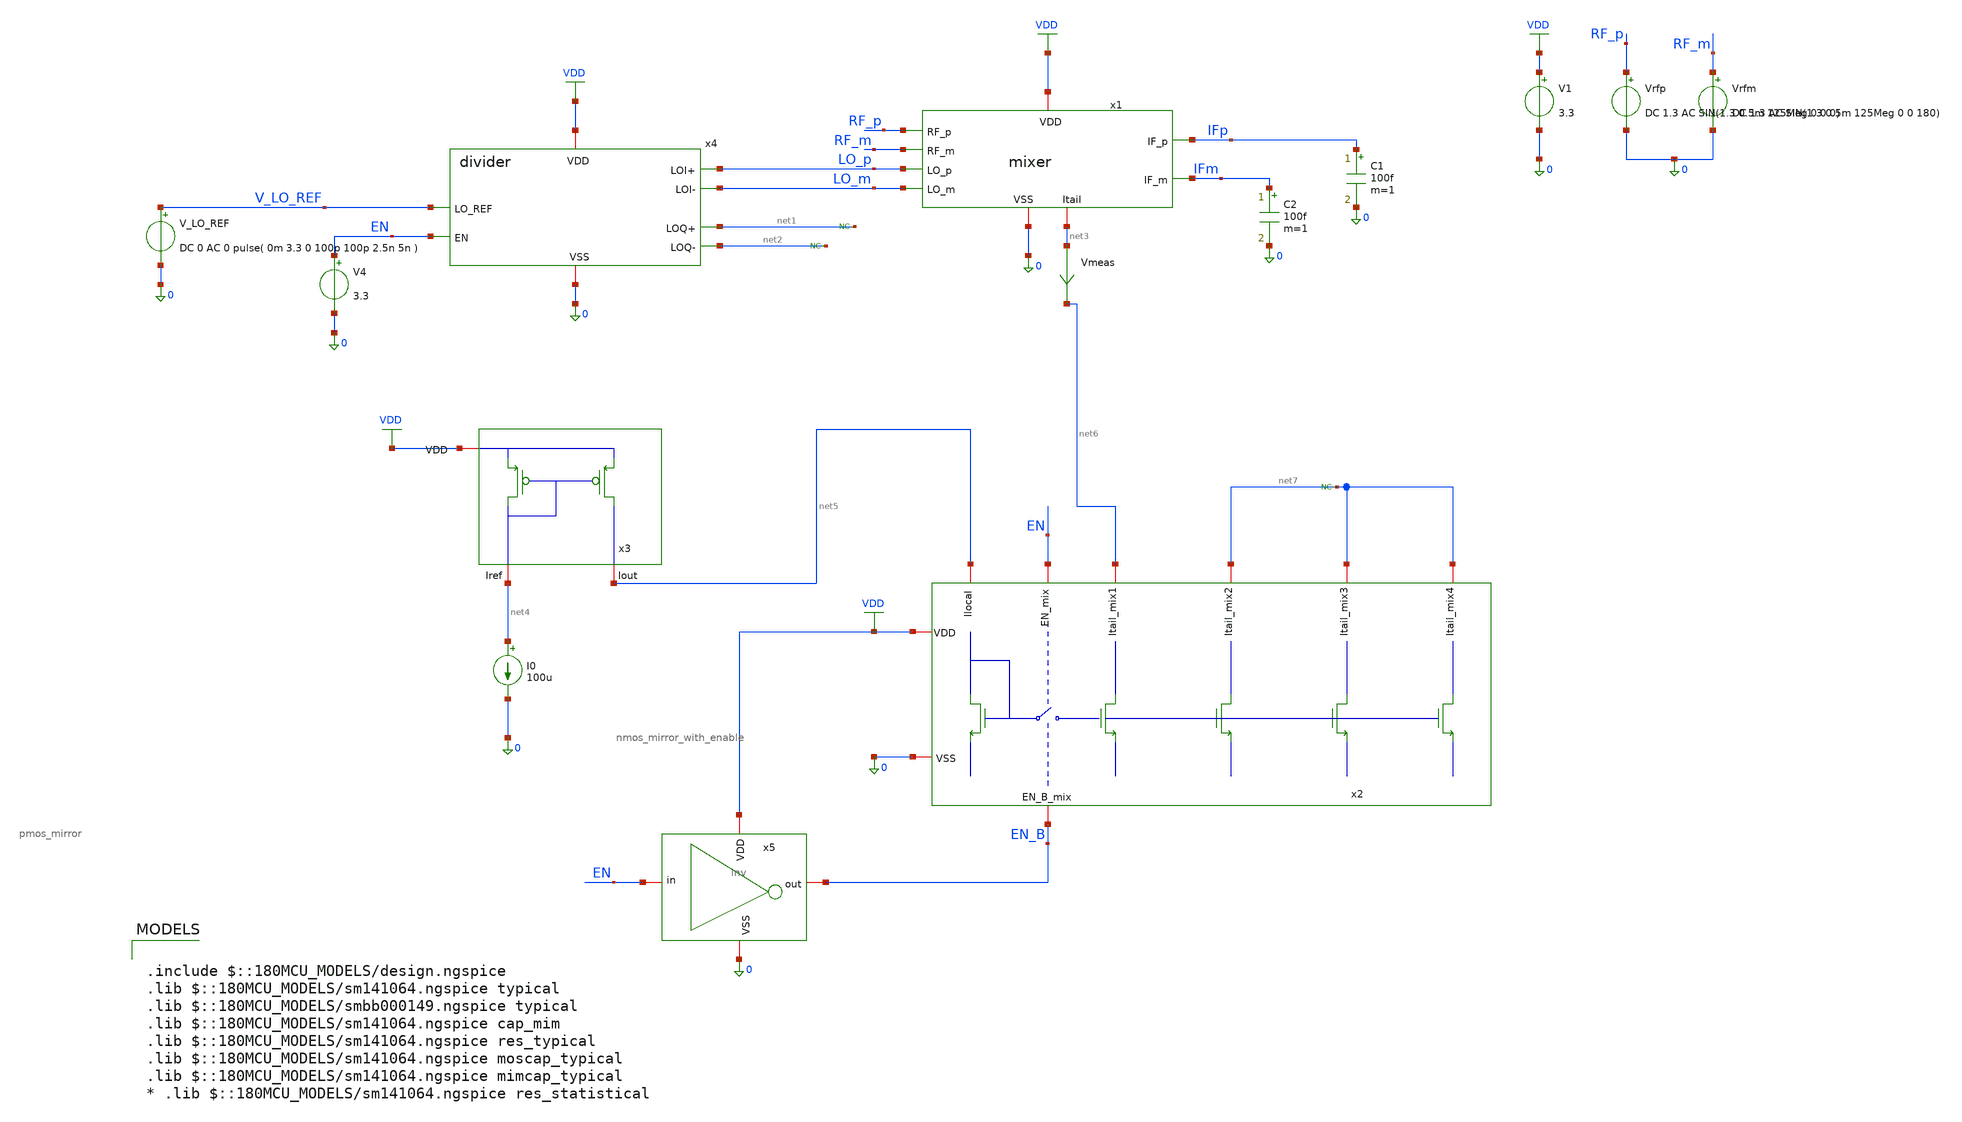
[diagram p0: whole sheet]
** sch_path: designs/top_level/testbench/mixer_and_divider.sch
**.subckt mixer_and_divider
V1 VDD 0 3.3
Vrfp RF_p 0 DC 1.3 AC SIN(1.3 0.5m 125Meg 0 0 0)
Vrfm RF_m 0 DC 1.3 AC SIN(1.3 0.5m 125Meg 0 0 180)
C1 IFp 0 100f m=1
C2 IFm 0 100f m=1
x1 IFp RF_p VDD 0 IFm RF_m LO_p net3 LO_m mixer
V_LO_REF V_LO_REF 0 DC 0 AC 0 pulse( 0m 3.3 0 100p 100p 2.5n 5n )
x4 VDD 0 V_LO_REF LO_p LO_m net1 net2 EN divider
* noconn #net1
* noconn #net2
V4 EN 0 3.3
x3 VDD net5 net4 pmos_mirror
I0 net4 0 100u
x2 net7 net7 net5 VDD EN net6 0 EN_B net7 nmos_mirror_with_enable
* noconn #net7
x5 VDD EN_B EN 0 inv
Vmeas net3 net6 0
.save i(vmeas)
**** begin user architecture code

.include $::180MCU_MODELS/design.ngspice
.lib $::180MCU_MODELS/sm141064.ngspice typical
.lib $::180MCU_MODELS/smbb000149.ngspice typical
.lib $::180MCU_MODELS/sm141064.ngspice cap_mim
.lib $::180MCU_MODELS/sm141064.ngspice res_typical
.lib $::180MCU_MODELS/sm141064.ngspice moscap_typical
.lib $::180MCU_MODELS/sm141064.ngspice mimcap_typical
* .lib $::180MCU_MODELS/sm141064.ngspice res_statistical




.control
op
destroy all
save all
write mixer_tb.raw


tran 0.01n 2u  ;transient sim

let vrf = V(RF_p)-V(RF_m)
let vlo = v(LO_p)-v(LO_m)
let vif = V(IFp)-V(IFm)

plot V(LO_p) V(LO_m)+3.3
plot vlo
plot vrf
plot V(RF_p) V(RF_m)+1m
plot vif
plot v(ifp)
plot i(vmeas)

fft V(LO_p) V(LO_m) vlo vif vrf

plot mag(vlo) vs frequency

plot mag(vif) vs frequency

plot mag(vrf) vs frequency
.endc


**** end user architecture code
**.ends
.GLOBAL VDD
.end
